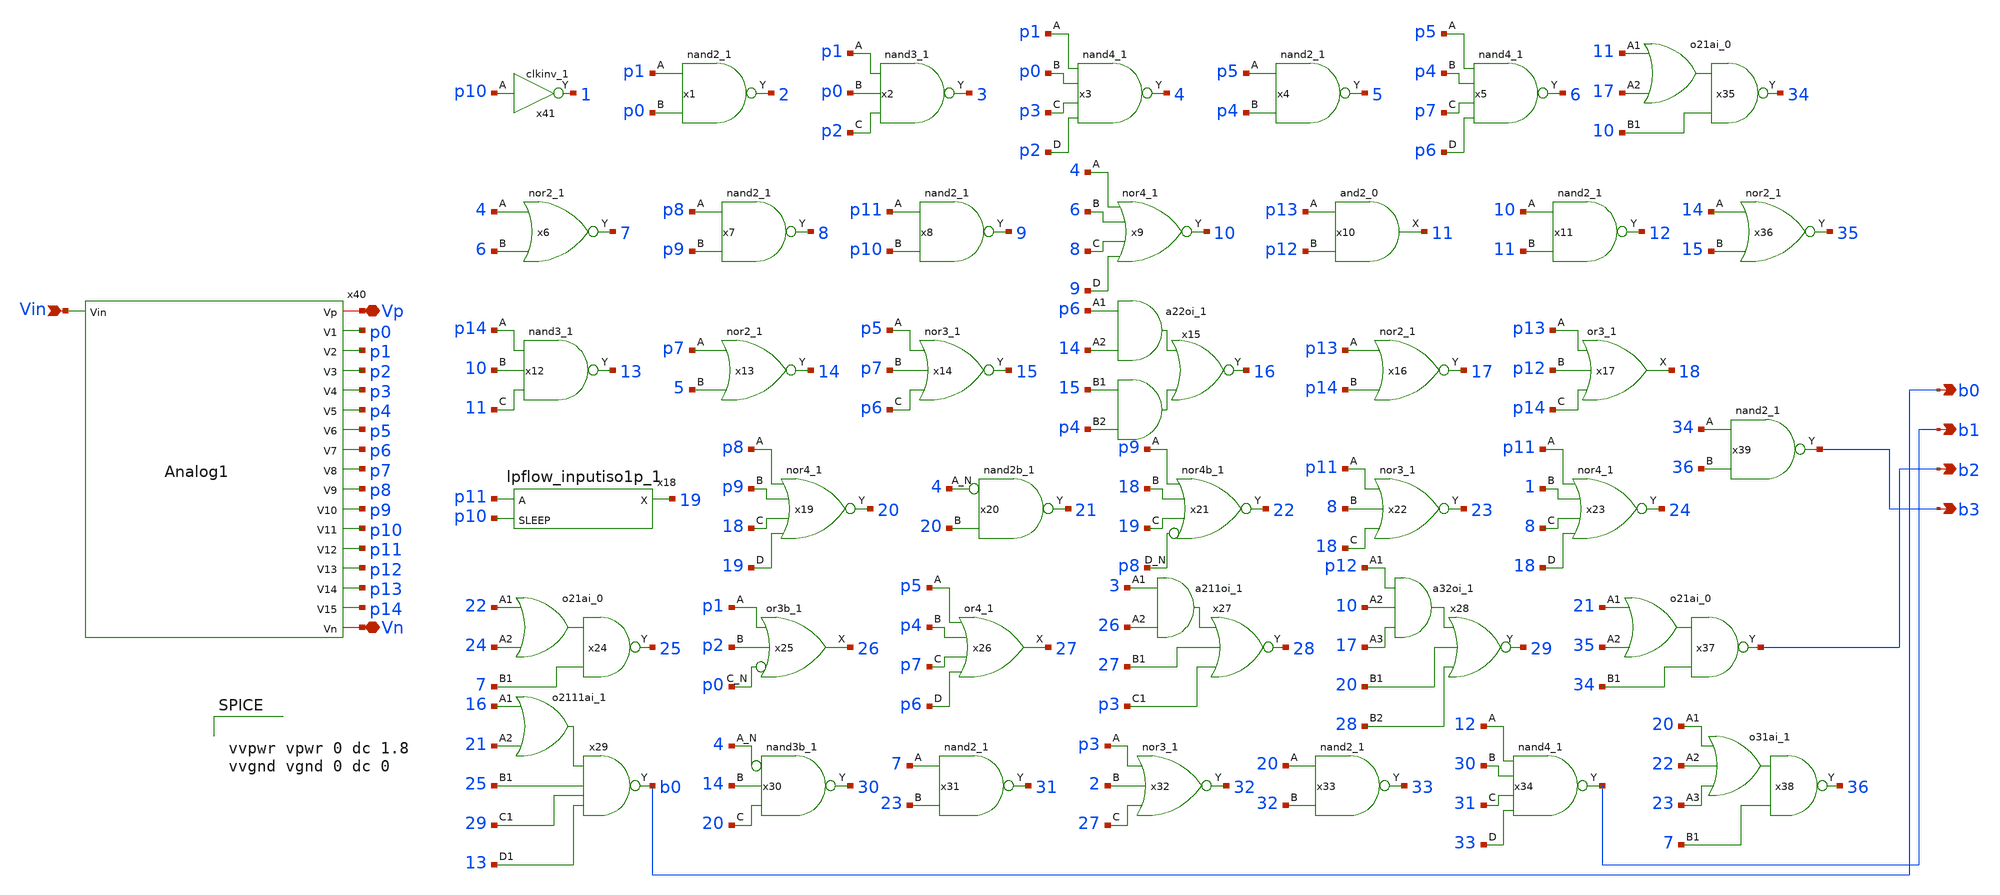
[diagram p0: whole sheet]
** sch_path: xschem/Vth_sch/Symbol/analog_therm.sch
**.subckt analog_therm b0 Vin b1 b2 b3 Vp Vn
*.opin b0
*.ipin Vin
*.opin b1
*.opin b2
*.opin b3
*.iopin Vp
*.iopin Vn
x1 p1 p0 VGND VNB VPB VPWR 2 sky130_fd_sc_hd__nand2_1
x2 p1 p0 p2 VGND VNB VPB VPWR 3 sky130_fd_sc_hd__nand3_1
x3 p1 p0 p3 p2 VGND VNB VPB VPWR 4 sky130_fd_sc_hd__nand4_1
x4 p5 p4 VGND VNB VPB VPWR 5 sky130_fd_sc_hd__nand2_1
x5 p5 p4 p7 p6 VGND VNB VPB VPWR 6 sky130_fd_sc_hd__nand4_1
x6 4 6 VGND VNB VPB VPWR 7 sky130_fd_sc_hd__nor2_1
x7 p8 p9 VGND VNB VPB VPWR 8 sky130_fd_sc_hd__nand2_1
x8 p11 p10 VGND VNB VPB VPWR 9 sky130_fd_sc_hd__nand2_1
x9 4 6 8 9 VGND VNB VPB VPWR 10 sky130_fd_sc_hd__nor4_1
x10 p13 p12 VGND VNB VPB VPWR 11 sky130_fd_sc_hd__and2_0
x11 10 11 VGND VNB VPB VPWR 12 sky130_fd_sc_hd__nand2_1
x12 p14 10 11 VGND VNB VPB VPWR 13 sky130_fd_sc_hd__nand3_1
x13 p7 5 VGND VNB VPB VPWR 14 sky130_fd_sc_hd__nor2_1
x14 p5 p7 p6 VGND VNB VPB VPWR 15 sky130_fd_sc_hd__nor3_1
x15 p6 14 15 p4 VGND VNB VPB VPWR 16 sky130_fd_sc_hd__a22oi_1
x16 p13 p14 VGND VNB VPB VPWR 17 sky130_fd_sc_hd__nor2_1
x17 p13 p12 p14 VGND VNB VPB VPWR 18 sky130_fd_sc_hd__or3_1
x18 p11 p10 VGND VNB VPB VPWR 19 sky130_fd_sc_hd__lpflow_inputiso1p_1
x19 p8 p9 18 19 VGND VNB VPB VPWR 20 sky130_fd_sc_hd__nor4_1
x20 4 20 VGND VNB VPB VPWR 21 sky130_fd_sc_hd__nand2b_1
x21 p9 18 19 p8 VGND VNB VPB VPWR 22 sky130_fd_sc_hd__nor4b_1
x22 p11 8 18 VGND VNB VPB VPWR 23 sky130_fd_sc_hd__nor3_1
x23 p11 1 8 18 VGND VNB VPB VPWR 24 sky130_fd_sc_hd__nor4_1
x24 22 24 7 VGND VNB VPB VPWR 25 sky130_fd_sc_hd__o21ai_0
x25 p1 p2 p0 VGND VNB VPB VPWR 26 sky130_fd_sc_hd__or3b_1
x26 p5 p4 p7 p6 VGND VNB VPB VPWR 27 sky130_fd_sc_hd__or4_1
x27 3 26 27 p3 VGND VNB VPB VPWR 28 sky130_fd_sc_hd__a211oi_1
x28 p12 10 17 20 28 VGND VNB VPB VPWR 29 sky130_fd_sc_hd__a32oi_1
x29 16 21 25 29 13 VGND VNB VPB VPWR b0 sky130_fd_sc_hd__o2111ai_1
x30 4 14 20 VGND VNB VPB VPWR 30 sky130_fd_sc_hd__nand3b_1
x31 7 23 VGND VNB VPB VPWR 31 sky130_fd_sc_hd__nand2_1
x32 p3 2 27 VGND VNB VPB VPWR 32 sky130_fd_sc_hd__nor3_1
x33 20 32 VGND VNB VPB VPWR 33 sky130_fd_sc_hd__nand2_1
x34 12 30 31 33 VGND VNB VPB VPWR b1 sky130_fd_sc_hd__nand4_1
x35 11 17 10 VGND VNB VPB VPWR 34 sky130_fd_sc_hd__o21ai_0
x36 14 15 VGND VNB VPB VPWR 35 sky130_fd_sc_hd__nor2_1
x37 21 35 34 VGND VNB VPB VPWR b2 sky130_fd_sc_hd__o21ai_0
x38 20 22 23 7 VGND VNB VPB VPWR 36 sky130_fd_sc_hd__o31ai_1
x39 34 36 VGND VNB VPB VPWR b3 sky130_fd_sc_hd__nand2_1
x40 Vin Vp p0 p1 p2 p3 p4 p5 p6 p7 p8 p9 p10 p11 p12 p13 p14 Vn Analog1
x41 p10 VGND VNB VPB VPWR 1 sky130_fd_sc_hd__clkinv_1
**** begin user architecture code


vvpwr vpwr 0 dc 1.8
vvgnd vgnd 0 dc 0


**** end user architecture code
**.ends
.end
